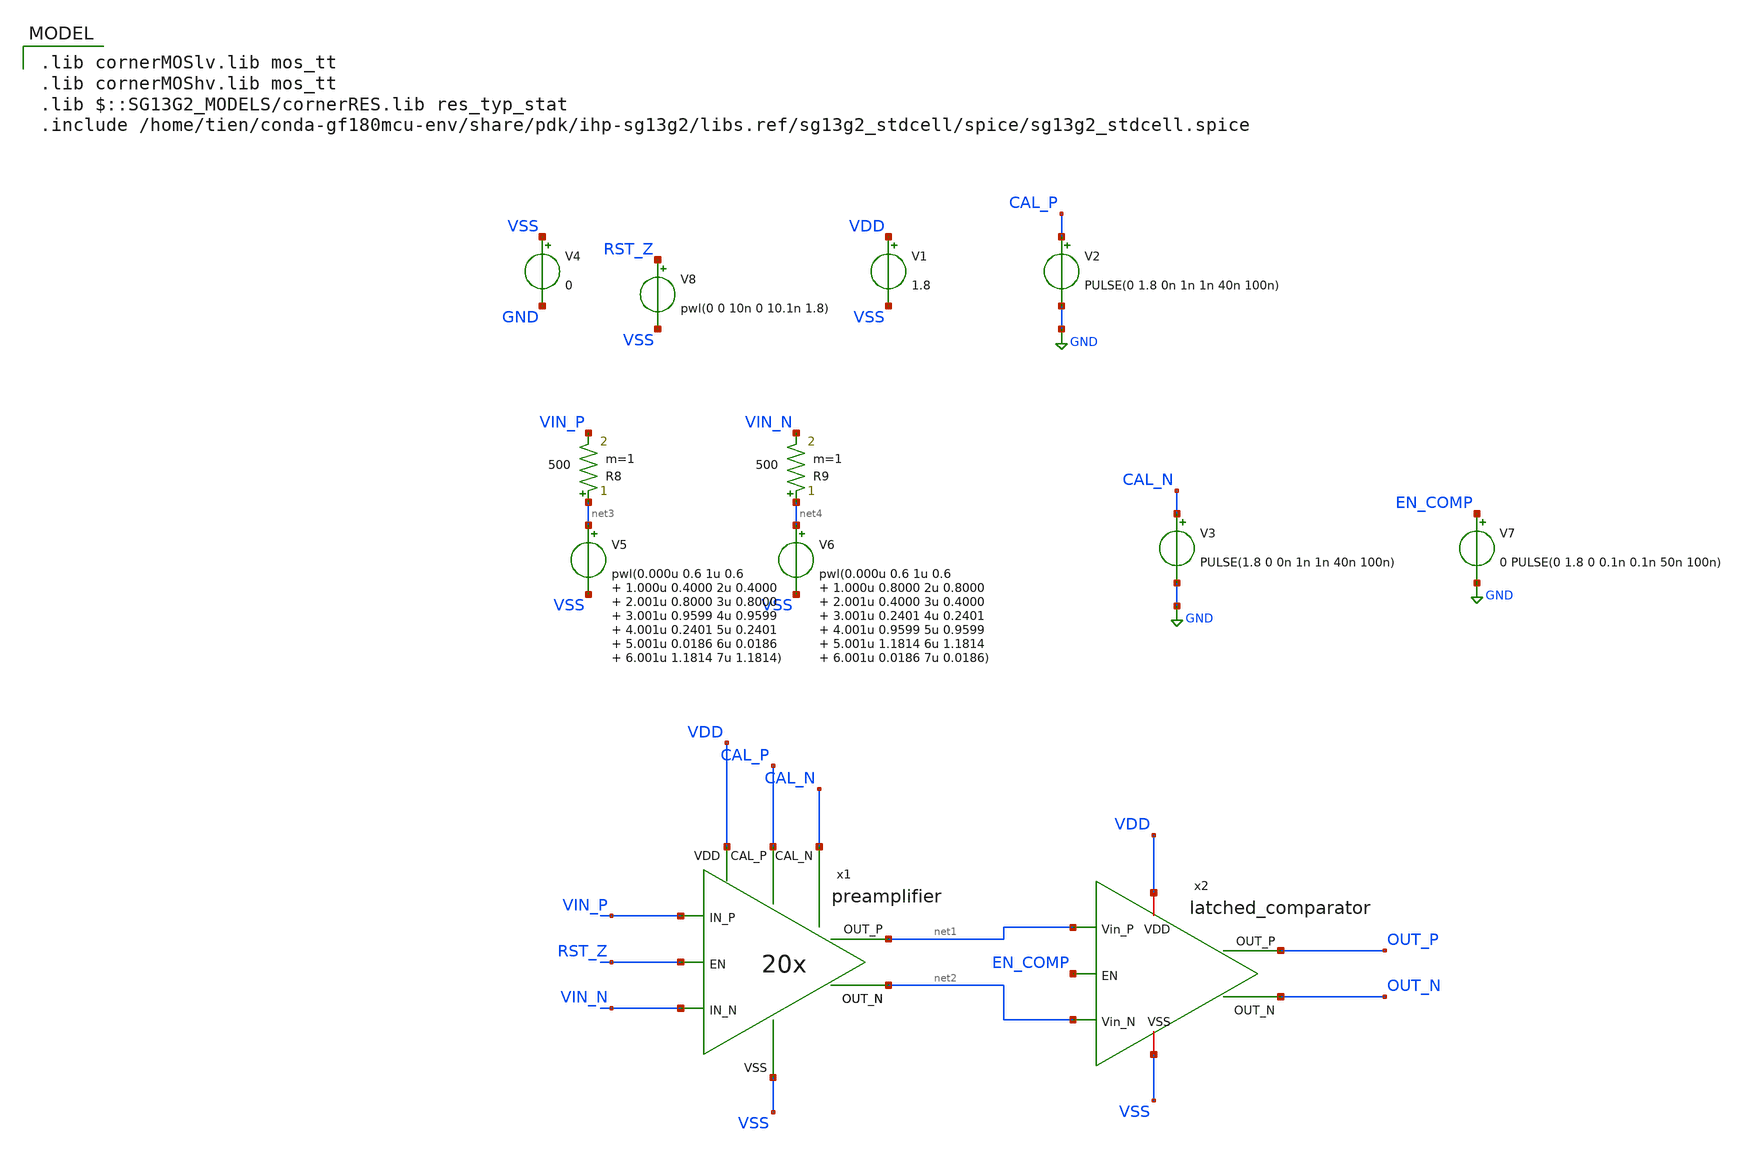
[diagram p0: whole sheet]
** sch_path: schematic/simulations/premamp_comparator_tb.sch
* IHP-GmbH/IHP-Open-PDK/ihp-sg13g2/libs.tech/xschem/sg13g2_stdcells/sg13g2_buf_4.sch:
* Copyright 2023 IHP PDK Authors
* Licensed under the Apache License, Version 2.0 (the "License");
**.subckt premamp_comparator_tb
x1 VIN_N VIN_P VDD RST_Z net1 net2 VSS CAL_P CAL_N preamplifier
x2 VDD net1 net2 OUT_P EN_COMP OUT_N VSS latched_comparator
V8 RST_Z VSS pwl(0 0 10n 0 10.1n 1.8)
V1 VDD VSS 1.8
.save i(v1)
V4 VSS GND 0
V5 net3 VSS pwl(0.000u 0.6 1u 0.6 1.000u 0.4000 2u 0.4000 2.001u 0.8000 3u 0.8000 3.001u 0.9599 4u
+ 0.9599 4.001u 0.2401 5u 0.2401 5.001u 0.0186 6u 0.0186 6.001u 1.1814 7u 1.1814)
V6 net4 VSS pwl(0.000u 0.6 1u 0.6 1.000u 0.8000 2u 0.8000 2.001u 0.4000 3u 0.4000 3.001u 0.2401 4u
+ 0.2401 4.001u 0.9599 5u 0.9599 5.001u 1.1814 6u 1.1814 6.001u 0.0186 7u 0.0186)
R8 net3 VIN_P 500 m=1
R9 net4 VIN_N 500 m=1
V2 CAL_P GND PULSE(0 1.8 0n 1n 1n 40n 100n)
V3 CAL_N GND PULSE(1.8 0 0n 1n 1n 40n 100n)
V7 EN_COMP GND 0 PULSE(0 1.8 0 0.1n 0.1n 50n 100n)
.save i(v7)
**** begin user architecture code
 .lib cornerMOSlv.lib mos_tt
.lib cornerMOShv.lib mos_tt
.lib $::SG13G2_MODELS/cornerRES.lib res_typ_stat
.include /home/tien/conda-gf180mcu-env/share/pdk/ihp-sg13g2/libs.ref/sg13g2_stdcell/spice/sg13g2_stdcell.spice




.option temp = 27
.save all

.option GMIN=1e-12 reltol=1e-6

.tran 10n 10u


**** end user architecture code
**.ends

* expanding   symbol:  preamplifier/preamplifier.sym # of pins=9
** sym_path: schematic/preamplifier/preamplifier.sym
** sch_path: schematic/preamplifier/preamplifier.sch
.subckt preamplifier IN_N IN_P VDD EN OUT_P OUT_N VSS CAL_P CAL_N
*.ipin VDD
*.ipin VSS
*.ipin IN_P
*.ipin IN_N
*.opin OUT_P
*.opin OUT_N
*.ipin EN
*.ipin CAL_P
*.ipin CAL_N
XM3 net1 net2 VDD VDD sg13_lv_pmos w=1.058u l=1u ng=1 m=6 mm_ok=1
XM2 net2 EN VDD VDD sg13_lv_pmos w=0.305u l=0.15u ng=1 m=1 mm_ok=1
XM5 VDD net2 VDD VDD sg13_lv_pmos w=1.058u l=1u ng=1 m=2 mm_ok=1
XM6 net4 net2 VDD VDD sg13_lv_pmos w=1.058u l=1u ng=1 m=1 mm_ok=1
XM1 net2 net2 VDD VDD sg13_lv_pmos w=1.058u l=1u ng=1 m=1 mm_ok=1
XM4 net8 net2 VDD VDD sg13_lv_pmos w=1.058u l=1u ng=1 m=3 mm_ok=1
XM7 net11 IN_P net1 VDD sg13_lv_pmos w=4.8u l=0.2u ng=2 m=4 mm_ok=1
XM8 net6 IN_N net1 VDD sg13_lv_pmos w=4.8u l=0.2u ng=2 m=4 mm_ok=1
XM9 OUT_P VSS net6 VDD sg13_hv_pmos w=14.6u l=0.4u ng=2 m=1 mm_ok=1
XM10 OUT_N VSS net11 VDD sg13_hv_pmos w=14.6u l=0.4u ng=2 m=1 mm_ok=1
XM11 net9 CAL_P net8 VDD sg13_lv_pmos w=1u l=1.77u ng=1 m=1 mm_ok=1
XM12 net10 CAL_N net8 VDD sg13_lv_pmos w=1u l=1.77u ng=1 m=1 mm_ok=1
XM13 net10 net5 VSS VSS sg13_lv_nmos w=1.118u l=0.15u ng=1 m=1 mm_ok=1
XM14 net9 net5 VSS VSS sg13_lv_nmos w=1.118u l=0.15u ng=1 m=1 mm_ok=1
XM15 net9 VSS VSS VSS sg13_lv_nmos w=1.118u l=0.15u ng=1 m=1 mm_ok=1
XM16 net10 VSS VSS VSS sg13_lv_nmos w=1.118u l=0.15u ng=1 m=1 mm_ok=1
XM17 net3 net3 VSS VSS sg13_lv_nmos w=0.9u l=0.15u ng=1 m=1 mm_ok=1
XM18 net5 net3 VSS VSS sg13_lv_nmos w=0.9u l=0.15u ng=1 m=2 mm_ok=1
XM19 VSS net3 VSS VSS sg13_lv_nmos w=0.9u l=0.15u ng=1 m=2 mm_ok=1
x1 EN_Z EN VDD VSS sg13g2_inv_1
XM20 OUT_P net4 net10 VSS sg13_lv_nmos w=0.9u l=0.15u ng=1 m=4 mm_ok=1
XM21 OUT_N net4 net9 VSS sg13_lv_nmos w=0.9u l=0.15u ng=1 m=4 mm_ok=1
XM22 net7 EN VSS VSS sg13_lv_nmos w=3.5u l=0.15u ng=1 m=1 mm_ok=1
XM23 net4 EN_Z VSS VSS sg13_lv_nmos w=0.42u l=0.15u ng=1 m=1 mm_ok=1
XM24 VDD OUT_N net5 VSS sg13_hv_nmos w=0.69u l=0.5u ng=1 m=1 rfmode=1 mm_ok=1
XM25 VDD OUT_P net5 VSS sg13_hv_nmos w=0.69u l=0.5u ng=1 m=1 rfmode=1 mm_ok=1
XR3 OUT_N rn[0] gnd rhigh w=0.5e-6 l=2.75e-6 m=1 b=0 mm_ok=1
XR1 rp[0] OUT_P gnd rhigh w=0.5e-6 l=2.75e-6 m=1 b=0 mm_ok=1
XR2 net14 net7 gnd rhigh w=0.5e-6 l=2.75e-6 m=1 b=0 mm_ok=1
XR4 net13 net14 gnd rhigh w=0.5e-6 l=2.75e-6 m=1 b=0 mm_ok=1
XR5 net12 net13 gnd rhigh w=0.5e-6 l=2.75e-6 m=1 b=0 mm_ok=1
XR6 net2 net12 gnd rhigh w=0.5e-6 l=2.75e-6 m=1 b=0 mm_ok=1
XR7 net15 net3 gnd rhigh w=0.5e-6 l=2.75e-6 m=1 b=0 mm_ok=1
XR8 net4 net15 gnd rhigh w=0.5e-6 l=2.75e-6 m=1 b=0 mm_ok=1
.ends


* expanding   symbol:  latched_comparator/latched_comparator.sym # of pins=7
** sym_path: schematic/latched_comparator/latched_comparator.sym
** sch_path: schematic/latched_comparator/latched_comparator.sch
.subckt latched_comparator VDD Vin_P Vin_N OUT_P EN OUT_N VSS
*.ipin Vin_P
*.ipin Vin_N
*.iopin VDD
*.iopin VSS
*.ipin EN
*.opin OUT_P
*.opin OUT_N
XM1 net1 ENi VDD VDD sg13_lv_pmos w=0.32u l=0.15u ng=1 m=1 mm_ok=1
XM2 OUT_Ni ENi VDD VDD sg13_lv_pmos w=0.32u l=0.15u ng=1 m=1 mm_ok=1
XM3 OUT_Ni OUT_Pi VDD VDD sg13_lv_pmos w=1.25u l=0.15u ng=1 m=1 mm_ok=1
XM4 net2 ENi VDD VDD sg13_lv_pmos w=0.32u l=0.15u ng=1 m=1 mm_ok=1
XM5 OUT_Pi ENi VDD VDD sg13_lv_pmos w=0.32u l=0.15u ng=1 m=1 mm_ok=1
XM6 OUT_Pi OUT_Ni VDD VDD sg13_lv_pmos w=1.25u l=0.15u ng=1 m=1 mm_ok=1
XM7 net1 Vin_P net3 VSS sg13_lv_nmos w=0.55u l=0.13u ng=1 m=1 mm_ok=1
XM8 net2 Vin_N net3 VSS sg13_lv_nmos w=0.55u l=0.13u ng=1 m=1 mm_ok=1
XM9 OUT_Pi OUT_Ni net2 VSS sg13_lv_nmos w=0.42u l=0.15u ng=1 m=1 mm_ok=1
XM10 OUT_Ni OUT_Pi net1 VSS sg13_lv_nmos w=0.42u l=0.15u ng=1 m=1 mm_ok=1
XM11 net3 net3 net3 VSS sg13_lv_nmos w=0.55u l=0.13u ng=1 m=2 mm_ok=1
XM12 net3 ENi VSS VSS sg13_lv_nmos w=0.9u l=0.15u ng=1 m=2 mm_ok=1
x4 net4 OUT_Pi VDD VSS sg13g2_inv_2
x5 net5 OUT_Ni VDD VSS sg13g2_inv_2
x1 ENi EN VDD VSS sg13g2_buf_4
x6 OUT_P net4 VDD VSS sg13g2_inv_4
x2 OUT_N net5 VDD VSS sg13g2_inv_4
.ends


* expanding   symbol:  sg13g2_stdcells/sg13g2_inv_1.sym # of pins=2
** sym_path: sg13g2_stdcells/sg13g2_inv_1.sym
** sch_path: sg13g2_stdcells/sg13g2_inv_1.sch
.subckt sg13g2_inv_1 Y A VDD VSS
*.opin Y
*.ipin A
*.iopin VDD
*.iopin VSS
XM1 Y A VSS VSS sg13_lv_nmos w=740.00n l=130.00n ng=1 m=1 mm_ok=1
XM2 Y A VDD VDD sg13_lv_pmos w=1.12u l=130.00n ng=1 m=1 mm_ok=1
.ends


* expanding   symbol:  sg13g2_stdcells/sg13g2_inv_2.sym # of pins=2
** sym_path: sg13g2_stdcells/sg13g2_inv_2.sym
** sch_path: sg13g2_stdcells/sg13g2_inv_2.sch
.subckt sg13g2_inv_2 Y A VDD VSS
*.opin Y
*.ipin A
*.iopin VDD
*.iopin VSS
XM1 Y A VSS VSS sg13_lv_nmos w=1.48u l=130.00n ng=2 m=1 mm_ok=1
XM2 Y A VDD VDD sg13_lv_pmos w=2.24u l=130.00n ng=2 m=1 mm_ok=1
.ends


* expanding   symbol:  sg13g2_stdcells/sg13g2_buf_4.sym # of pins=2
** sym_path: sg13g2_stdcells/sg13g2_buf_4.sym
** sch_path: sg13g2_stdcells/sg13g2_buf_4.sch
.subckt sg13g2_buf_4 X A VDD VSS
*.ipin A
*.opin X
*.iopin VDD
*.iopin VSS
XM1 net1 A VSS VSS sg13_lv_nmos w=740.00n l=130.00n ng=1 m=1 mm_ok=1
XM2 X net1 VSS VSS sg13_lv_nmos w=2.96u l=130.00n ng=4 m=1 mm_ok=1
XM3 net1 A VDD VDD sg13_lv_pmos w=1.68u l=130.00n ng=2 m=1 mm_ok=1
XM4 X net1 VDD VDD sg13_lv_pmos w=4.48u l=130.00n ng=4 m=1 mm_ok=1
.ends


* expanding   symbol:  sg13g2_stdcells/sg13g2_inv_4.sym # of pins=2
** sym_path: sg13g2_stdcells/sg13g2_inv_4.sym
** sch_path: sg13g2_stdcells/sg13g2_inv_4.sch
.subckt sg13g2_inv_4 Y A VDD VSS
*.ipin A
*.opin Y
*.iopin VDD
*.iopin VSS
XM1 Y A VSS VSS sg13_lv_nmos w=2.96u l=130.00n ng=4 m=1 mm_ok=1
XM2 Y A VDD VDD sg13_lv_pmos w=4.48u l=130.00n ng=4 m=1 mm_ok=1
.ends

.GLOBAL GND
.end
